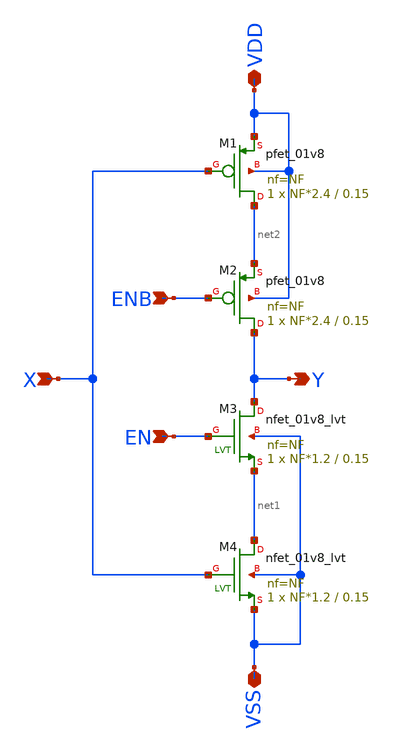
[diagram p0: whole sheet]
** sch_path: xschem_lib/DFFRAM_full_custom/tinv.sch
**.subckt tinv X ENB EN Y VDD VSS
*.ipin X
*.ipin ENB
*.ipin EN
*.opin Y
*.iopin VDD
*.iopin VSS
XM1 net2 X VDD VDD sky130_fd_pr__pfet_01v8 L=0.15 W=NF*2.4 nf=NF ad='int((nf+1)/2) * W/nf * 0.29' as='int((nf+2)/2) * W/nf * 0.29'
+ pd='2*int((nf+1)/2) * (W/nf + 0.29)' ps='2*int((nf+2)/2) * (W/nf + 0.29)' nrd='0.29 / W' nrs='0.29 / W'
+ sa=0 sb=0 sd=0 mult=1 m=1
XM3 Y EN net1 VSS sky130_fd_pr__nfet_01v8_lvt L=0.15 W=NF*1.2 nf=NF ad='int((nf+1)/2) * W/nf * 0.29'
+ as='int((nf+2)/2) * W/nf * 0.29' pd='2*int((nf+1)/2) * (W/nf + 0.29)' ps='2*int((nf+2)/2) * (W/nf + 0.29)'
+ nrd='0.29 / W' nrs='0.29 / W' sa=0 sb=0 sd=0 mult=1 m=1
XM2 Y ENB net2 VDD sky130_fd_pr__pfet_01v8 L=0.15 W=NF*2.4 nf=NF ad='int((nf+1)/2) * W/nf * 0.29' as='int((nf+2)/2) * W/nf * 0.29'
+ pd='2*int((nf+1)/2) * (W/nf + 0.29)' ps='2*int((nf+2)/2) * (W/nf + 0.29)' nrd='0.29 / W' nrs='0.29 / W'
+ sa=0 sb=0 sd=0 mult=1 m=1
XM4 net1 X VSS VSS sky130_fd_pr__nfet_01v8_lvt L=0.15 W=NF*1.2 nf=NF ad='int((nf+1)/2) * W/nf * 0.29'
+ as='int((nf+2)/2) * W/nf * 0.29' pd='2*int((nf+1)/2) * (W/nf + 0.29)' ps='2*int((nf+2)/2) * (W/nf + 0.29)'
+ nrd='0.29 / W' nrs='0.29 / W' sa=0 sb=0 sd=0 mult=1 m=1
**.ends
.end
